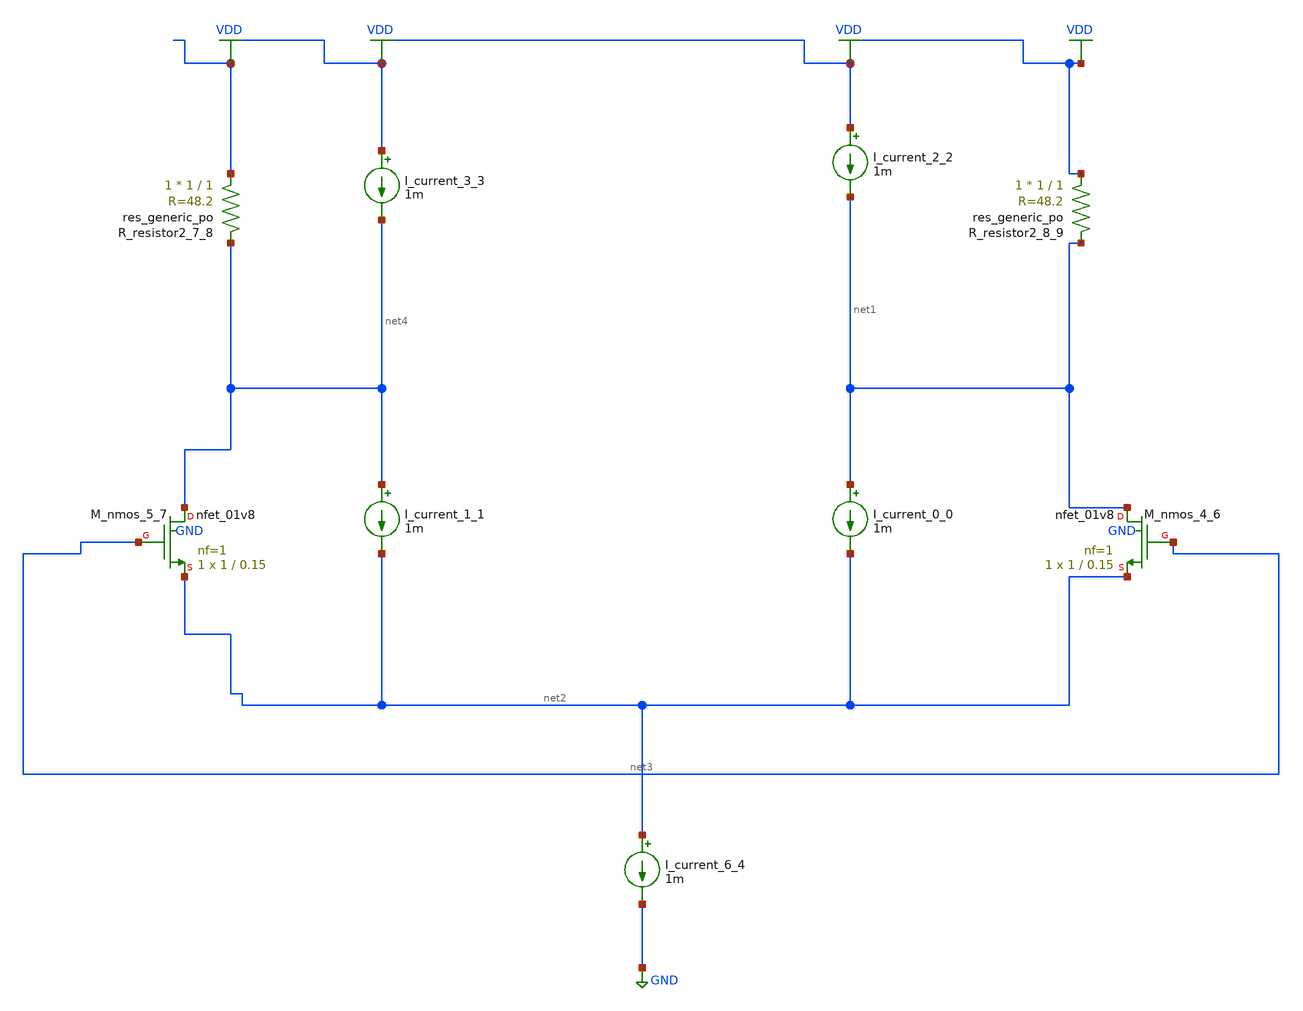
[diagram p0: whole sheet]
** sch_path: schematics/AMSNet/481.sch
**.subckt 481
I_current_0_0 net1 net2 1m
I_current_1_1 net4 net2 1m
I_current_2_2 VDD net1 1m
I_current_3_3 VDD net4 1m
I_current_6_4 net2 GND 1m
XM_nmos_4_6 net1 net3 net2 GND sky130_fd_pr__nfet_01v8 L=0.15 W=1 nf=1 ad='int((1 + 1)/2) * 1 / 1 * 0.29'
+ as='int((1 + 2)/2) * 1 / 1 * 0.29' pd='2*int((1 + 1)/2) * (1 / 1 + 0.29)' ps='2*int((1 + 2)/2) * (1 / 1 + 0.29)'
+ nrd='0.29 / 1 ' nrs='0.29 / 1 ' sa=0 sb=0 sd=0 mult=1 m=1
XM_nmos_5_7 net4 net3 net2 GND sky130_fd_pr__nfet_01v8 L=0.15 W=1 nf=1 ad='int((1 + 1)/2) * 1 / 1 * 0.29'
+ as='int((1 + 2)/2) * 1 / 1 * 0.29' pd='2*int((1 + 1)/2) * (1 / 1 + 0.29)' ps='2*int((1 + 2)/2) * (1 / 1 + 0.29)'
+ nrd='0.29 / 1 ' nrs='0.29 / 1 ' sa=0 sb=0 sd=0 mult=1 m=1
XR_resistor2_7_8 VDD net4 sky130_fd_pr__res_generic_po W=1 L=1 m=1
XR_resistor2_8_9 VDD net1 sky130_fd_pr__res_generic_po W=1 L=1 m=1
**.ends
.GLOBAL GND
.GLOBAL VDD
.end
